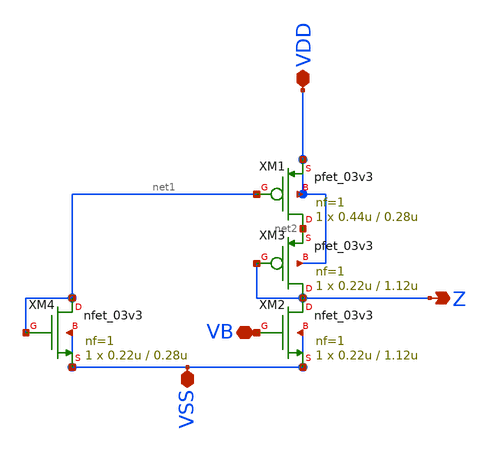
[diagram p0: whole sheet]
** sch_path: xschem_sn2/TIEM.sch
**.subckt TIEM VSS VDD Z VB
*.iopin VSS
*.iopin VDD
*.opin Z
*.iopin VB
XM1 net2 net1 VDD VDD pfet_03v3 L=0.28u W=0.44u nf=1 ad='int((nf+1)/2) * W/nf * 0.18u' as='int((nf+2)/2) * W/nf * 0.18u'
+ pd='2*int((nf+1)/2) * (W/nf + 0.18u)' ps='2*int((nf+2)/2) * (W/nf + 0.18u)' nrd='0.18u / W' nrs='0.18u / W'
+ sa=0 sb=0 sd=0 m=1 par=1
XM2 Z VB VSS VSS nfet_03v3 L=1.12u W=0.22u nf=1 ad='int((nf+1)/2) * W/nf * 0.18u' as='int((nf+2)/2) * W/nf * 0.18u'
+ pd='2*int((nf+1)/2) * (W/nf + 0.18u)' ps='2*int((nf+2)/2) * (W/nf + 0.18u)' nrd='0.18u / W' nrs='0.18u / W'
+ sa=0 sb=0 sd=0 m=1 par=1
XM3 Z Z net2 VDD pfet_03v3 L=1.12u W=0.22u nf=1 ad='int((nf+1)/2) * W/nf * 0.18u' as='int((nf+2)/2) * W/nf * 0.18u'
+ pd='2*int((nf+1)/2) * (W/nf + 0.18u)' ps='2*int((nf+2)/2) * (W/nf + 0.18u)' nrd='0.18u / W' nrs='0.18u / W'
+ sa=0 sb=0 sd=0 m=1 par=1
XM4 net1 net1 VSS VSS nfet_03v3 L=0.28u W=0.22u nf=1 ad='int((nf+1)/2) * W/nf * 0.18u' as='int((nf+2)/2) * W/nf * 0.18u'
+ pd='2*int((nf+1)/2) * (W/nf + 0.18u)' ps='2*int((nf+2)/2) * (W/nf + 0.18u)' nrd='0.18u / W' nrs='0.18u / W'
+ sa=0 sb=0 sd=0 m=1 par=1
**.ends
.end
